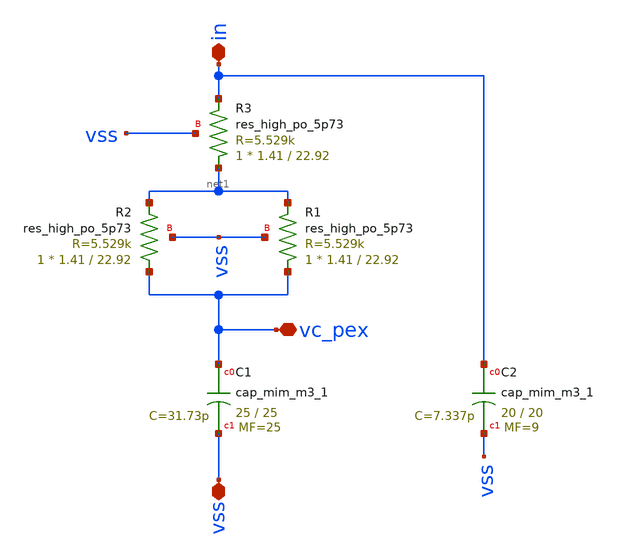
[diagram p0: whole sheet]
** sch_path: xschem/loop_filter.sch
**.subckt loop_filter in vss vc_pex
*.iopin in
*.iopin vss
*.iopin vc_pex
XC1 vc_pex vss sky130_fd_pr__cap_mim_m3_1 W=25 L=25 MF=25 m=25
XC2 in vss sky130_fd_pr__cap_mim_m3_1 W=20 L=20 MF=9 m=9
XR2 vc_pex net1 vss sky130_fd_pr__res_high_po_5p73 L=22.92 mult=1 m=1
XR1 vc_pex net1 vss sky130_fd_pr__res_high_po_5p73 L=22.92 mult=1 m=1
XR3 net1 in vss sky130_fd_pr__res_high_po_5p73 L=22.92 mult=1 m=1
**.ends
.end
